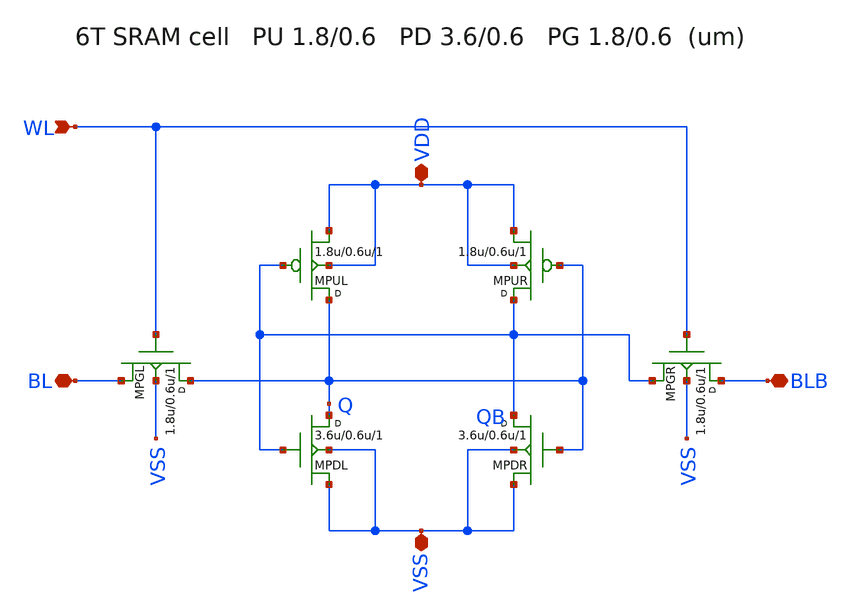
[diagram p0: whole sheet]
** sch_path: sch/sram6t.sch
**.subckt sram6t WL BL BLB VDD VSS
*.ipin WL
*.iopin BL
*.iopin BLB
*.iopin VDD
*.iopin VSS
MPUL Q QB VDD VDD pfet w=1.8u l=0.6u m=1
MPDL Q QB VSS VSS nfet w=3.6u l=0.6u m=1
MPUR QB Q VDD VDD pfet w=1.8u l=0.6u m=1
MPDR QB Q VSS VSS nfet w=3.6u l=0.6u m=1
MPGL Q WL BL VSS nfet w=1.8u l=0.6u m=1
MPGR BLB WL QB VSS nfet w=1.8u l=0.6u m=1
**.ends
.end
